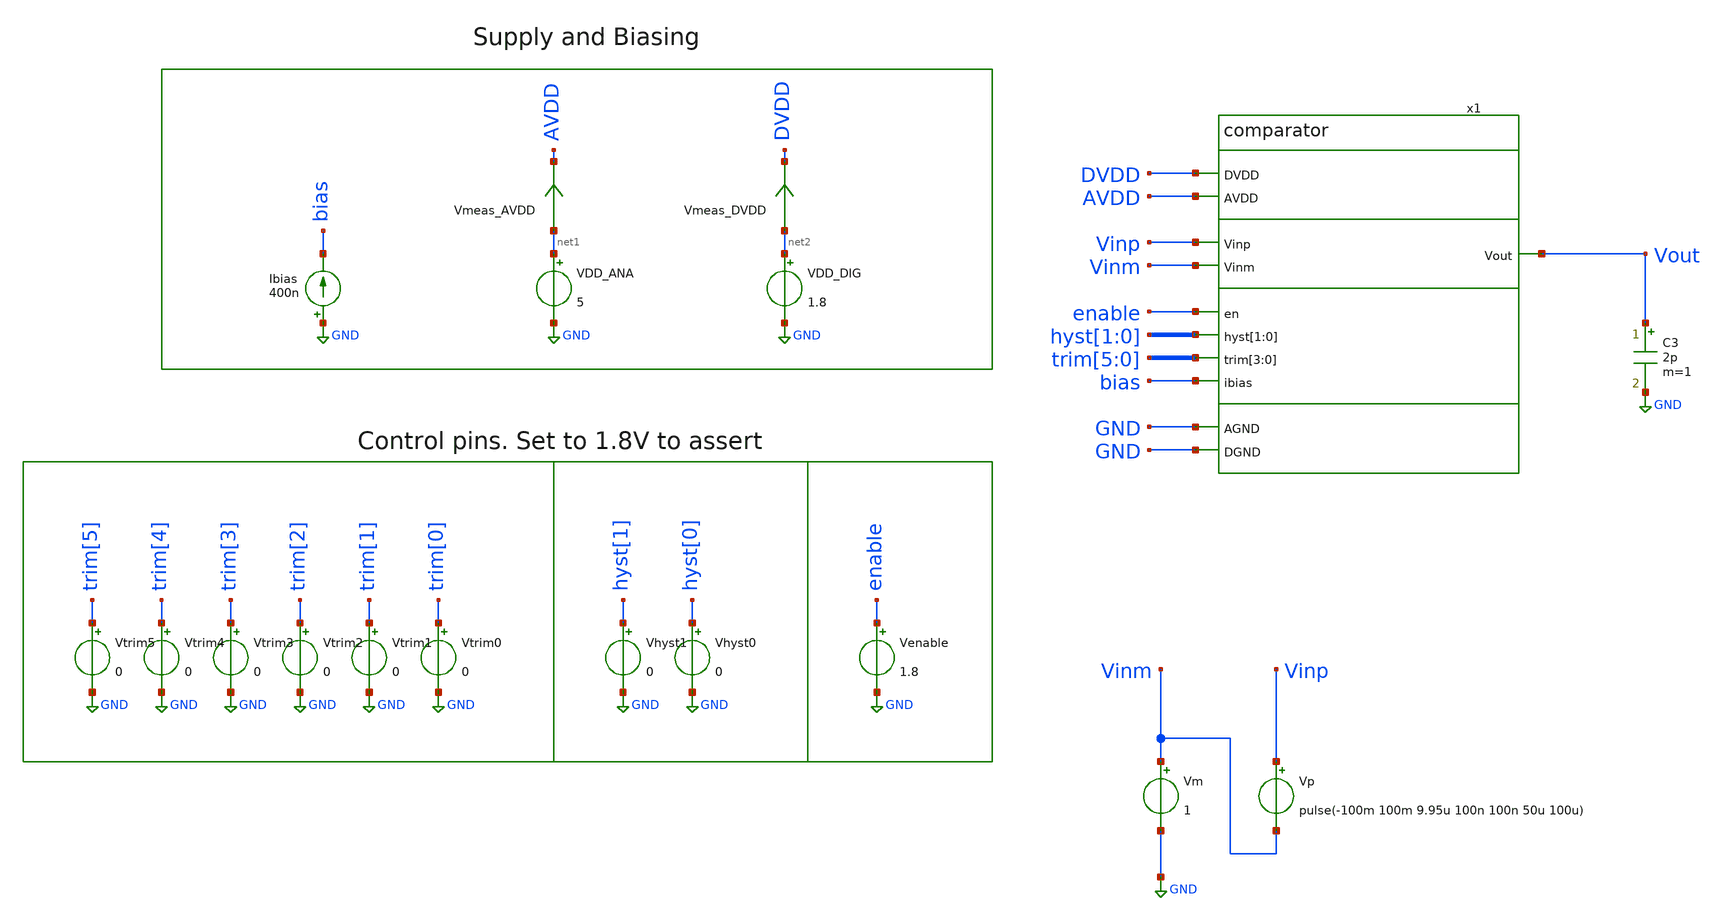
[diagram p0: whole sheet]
** sch_path: xschem/tb_comparator_delay.sch
**.subckt tb_comparator_delay
Vp Vinp Vinm pulse(-100m 100m 9.95u 100n 100n 50u 100u)
VDD_ANA net1 GND 5
VDD_DIG net2 GND 1.8
Ibias GND bias 400n
C3 Vout GND 2p m=1
Vm Vinm GND 1
Vmeas_AVDD net1 AVDD 0
.save i(vmeas_avdd)
Vmeas_DVDD net2 DVDD 0
.save i(vmeas_dvdd)
Vtrim3 trim[3] GND 0
Vtrim2 trim[2] GND 0
Vtrim1 trim[1] GND 0
Vtrim0 trim[0] GND 0
Vhyst1 hyst[1] GND 0
Vhyst0 hyst[0] GND 0
Venable enable GND 1.8
Vtrim5 trim[5] GND 0
Vtrim4 trim[4] GND 0
x1 DVDD AVDD GND GND Vinp Vout Vinm enable hyst[1] hyst[0] trim[5] trim[4] trim[3] trim[2] bias
+ comparator
**** begin user architecture code
.lib $::SKYWATER_MODELS/sky130.lib.spice fs


*.include /foss/designs/sky130_ak_ip__comparator/mag/comparator_rcx.spice
.save v(vout)
.tran 3n 12u 9.5u
.ic v(x1.vop)=0 v(x1.vdiff)=1.8 v(x1.vout_int)=0 v(x1.voutb)=1.8 v(vout)=0
.control
let vec=unitvec(1)
let num_meas = 45
let propdelay = unitvec(num_meas)
let x = unitvec(num_meas)
let i = 0
foreach temp_val -40 27 85
   set temp=$temp_val
   foreach vdd_ana_val 2.95 3.3 5.5
      alter VDD_ANA $vdd_ana_val
      foreach vm_val 0.1 {$vdd_ana_val*0.25} {$vdd_ana_val/2} {$vdd_ana_val*0.75} {-0.1+$vdd_ana_val}
         alter Vm $vm_val
         run
         meas tran t_cross when v(vout)=0.9 rise=1
         let delay = t_cross - 10e-6
         let propdelay[i] = delay
         set filetype=ascii
         set appendwrite
         set wr_singlescale
         setscale vec
         wrdata results_delay.out delay
         let i = i+1
      end
   end
end
print vecmax(propdelay)
print vecmin(propdelay)
.endc


**** end user architecture code
**.ends
.GLOBAL GND
.end
